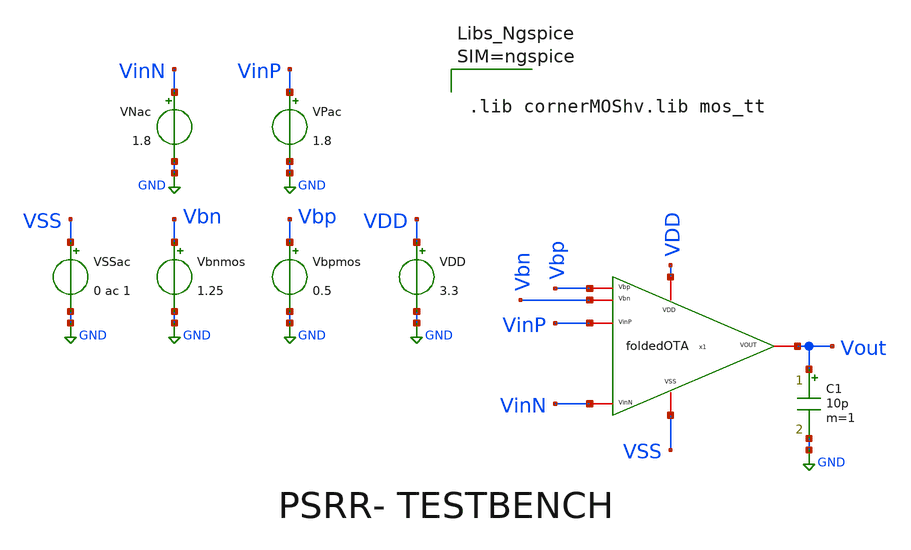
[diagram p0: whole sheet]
** sch_path: psrr/PSRRn-foldedOTA.sch
* v1_ideal_current_sources/schematic/foldedOTA.sch:
* (c) 2026 Fares Satouh
**.subckt PSRRn-foldedOTA
VPac VinP GND 1.8
VNac VinN GND 1.8
Vbnmos Vbn GND 1.25
Vbpmos Vbp GND 0.5
VDD VDD GND 3.3
x1 VDD Vbp Vout VinP VinN Vbn VSS foldedOTA
C1 Vout GND 10p m=1
VSSac VSS GND 0 ac 1
**** begin user architecture code



.lib cornerMOShv.lib mos_tt





.control
close all
destroy all

ac dec 20 1 200G
let gain_vss_db = db(Vout/v(VSS))
meas ac avss_dc_gain find gain_vss_db at=1

alter VPac ac = 100m
alter VNac ac = -100m
alter VSSac ac = 0
ac dec 20 1 200G
let VinDiff = v(VinP) - v(VinN)
let gain_dm_db = db(Vout/VinDiff)
meas ac adm_dc_gain find gain_dm_db at=1

let psrr_neg_dc = adm_dc_gain - ac1.avss_dc_gain
let psrr_neg_full = gain_dm_db - ac1.gain_vss_db

print adm_dc_gain
print ac1.avss_dc_gain
print psrr_neg_dc

plot ac1.gain_vss_db gain_dm_db
plot psrr_neg_full
.endc


**** end user architecture code
**.ends

* expanding   symbol:  foldedOTA.sym # of pins=7
** sym_path: v1_ideal_current_sources/schematic/foldedOTA.sym
** sch_path: v1_ideal_current_sources/schematic/foldedOTA.sch
.subckt foldedOTA VDD Vbp VOUT VinP VinN Vbn VSS
*.iopin VDD
*.iopin VSS
*.iopin VOUT
*.iopin Vbp
*.iopin Vbn
*.iopin VinN
*.iopin VinP
XM1 net2 VinP net1 VSS sg13_hv_nmos w=28u l=1u ng=4 m=1 mm_ok=1
XM2 net3 VinN net1 VSS sg13_hv_nmos w=28u l=1u ng=4 m=1 mm_ok=1
XM3 net1 net8 VSS VSS sg13_hv_nmos w=15u l=1u ng=3 m=1 mm_ok=1
XM4 net2 net7 VDD VDD sg13_hv_pmos w=14u l=1u ng=2 m=1 mm_ok=1
XM5 net3 net7 VDD VDD sg13_hv_pmos w=14u l=1u ng=2 m=1 mm_ok=1
XM6 net4 Vbp net2 VDD sg13_hv_pmos w=2u l=1u ng=1 m=1 mm_ok=1
XM7 VOUT Vbp net3 VDD sg13_hv_pmos w=2u l=1u ng=1 m=1 mm_ok=1
XM8 net4 Vbn net5 VSS sg13_hv_nmos w=7u l=1u ng=1 m=1 mm_ok=1
XM9 VOUT Vbn net6 VSS sg13_hv_nmos w=7u l=1u ng=1 m=1 mm_ok=1
XM10 net5 net4 VSS VSS sg13_hv_nmos w=7u l=1u ng=1 m=1 mm_ok=1
XM11 net6 net4 VSS VSS sg13_hv_nmos w=7u l=1u ng=1 m=1 mm_ok=1
XM12 net8 net8 VSS VSS sg13_hv_nmos w=15u l=1u ng=3 m=1 mm_ok=1
I0 VDD net8 50u
XM13 net7 net7 VDD VDD sg13_hv_pmos w=14u l=1u ng=2 m=1 mm_ok=1
I1 net7 VSS 50u
.ends

.GLOBAL GND
.end
